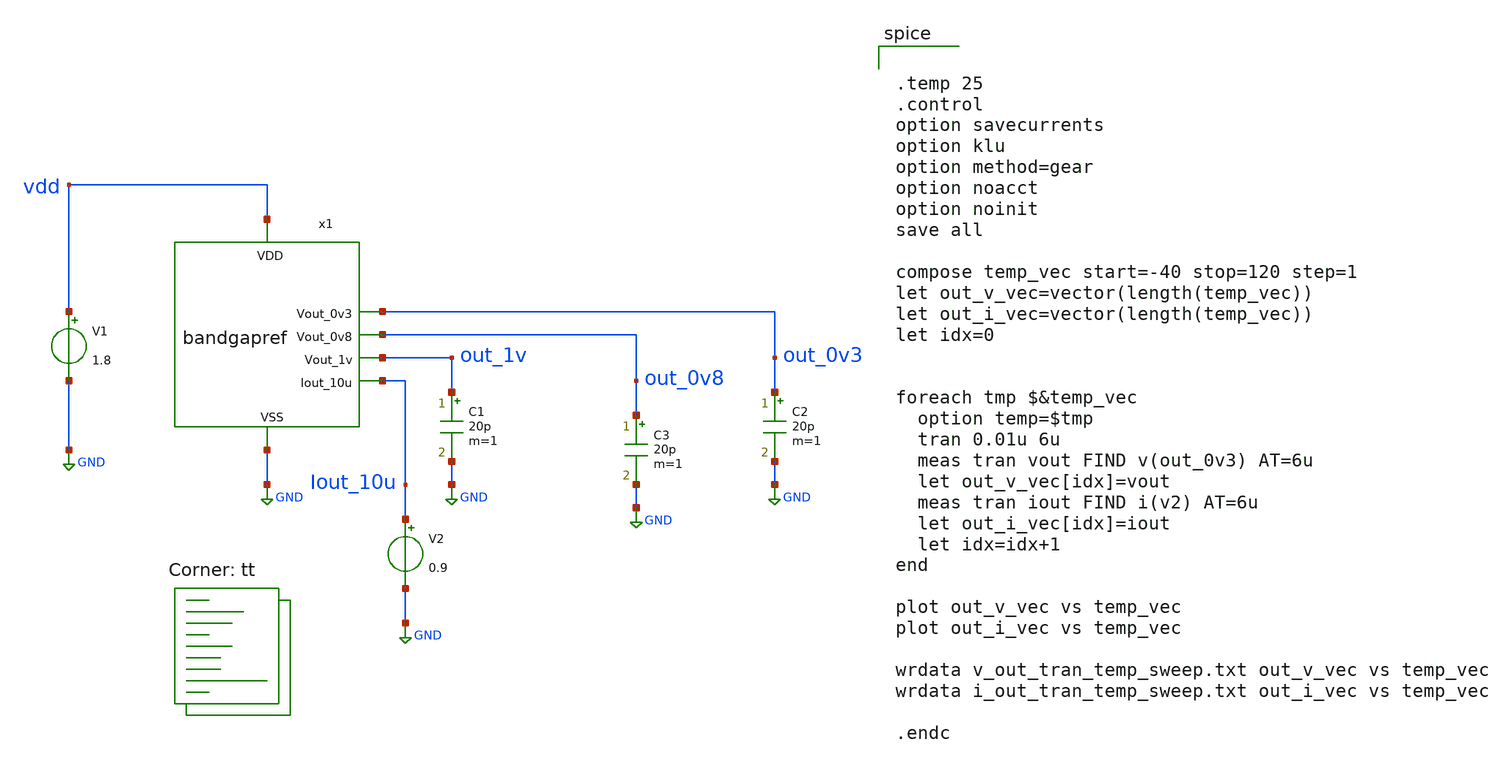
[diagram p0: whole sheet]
** sch_path: xschem/bandgapref_tran_temp_sweep_tb.sch
**.subckt bandgapref_tran_temp_sweep_tb
V1 vdd GND 1.8
.save i(v1)
x1 vdd out_0v3 GND out_1v out_0v8 Iout_10u bandgapref
C1 out_1v GND 20p m=1
C2 out_0v3 GND 20p m=1
C3 out_0v8 GND 20p m=1
V2 Iout_10u GND 0.9
.save i(v2)
**** begin user architecture code
.lib $::SKYWATER_MODELS/sky130.lib.spice tt


.temp 25
.control
option savecurrents
option klu
option method=gear
option noacct
option noinit
save all

compose temp_vec start=-40 stop=120 step=1
let out_v_vec=vector(length(temp_vec))
let out_i_vec=vector(length(temp_vec))
let idx=0


foreach tmp $&temp_vec
  option temp=$tmp
  tran 0.01u 6u
  meas tran vout FIND v(out_0v3) AT=6u
  let out_v_vec[idx]=vout
  meas tran iout FIND i(v2) AT=6u
  let out_i_vec[idx]=iout
  let idx=idx+1
end

plot out_v_vec vs temp_vec
plot out_i_vec vs temp_vec

wrdata v_out_tran_temp_sweep.txt out_v_vec vs temp_vec
wrdata i_out_tran_temp_sweep.txt out_i_vec vs temp_vec

.endc

**** end user architecture code
**.ends
.GLOBAL GND
.end
